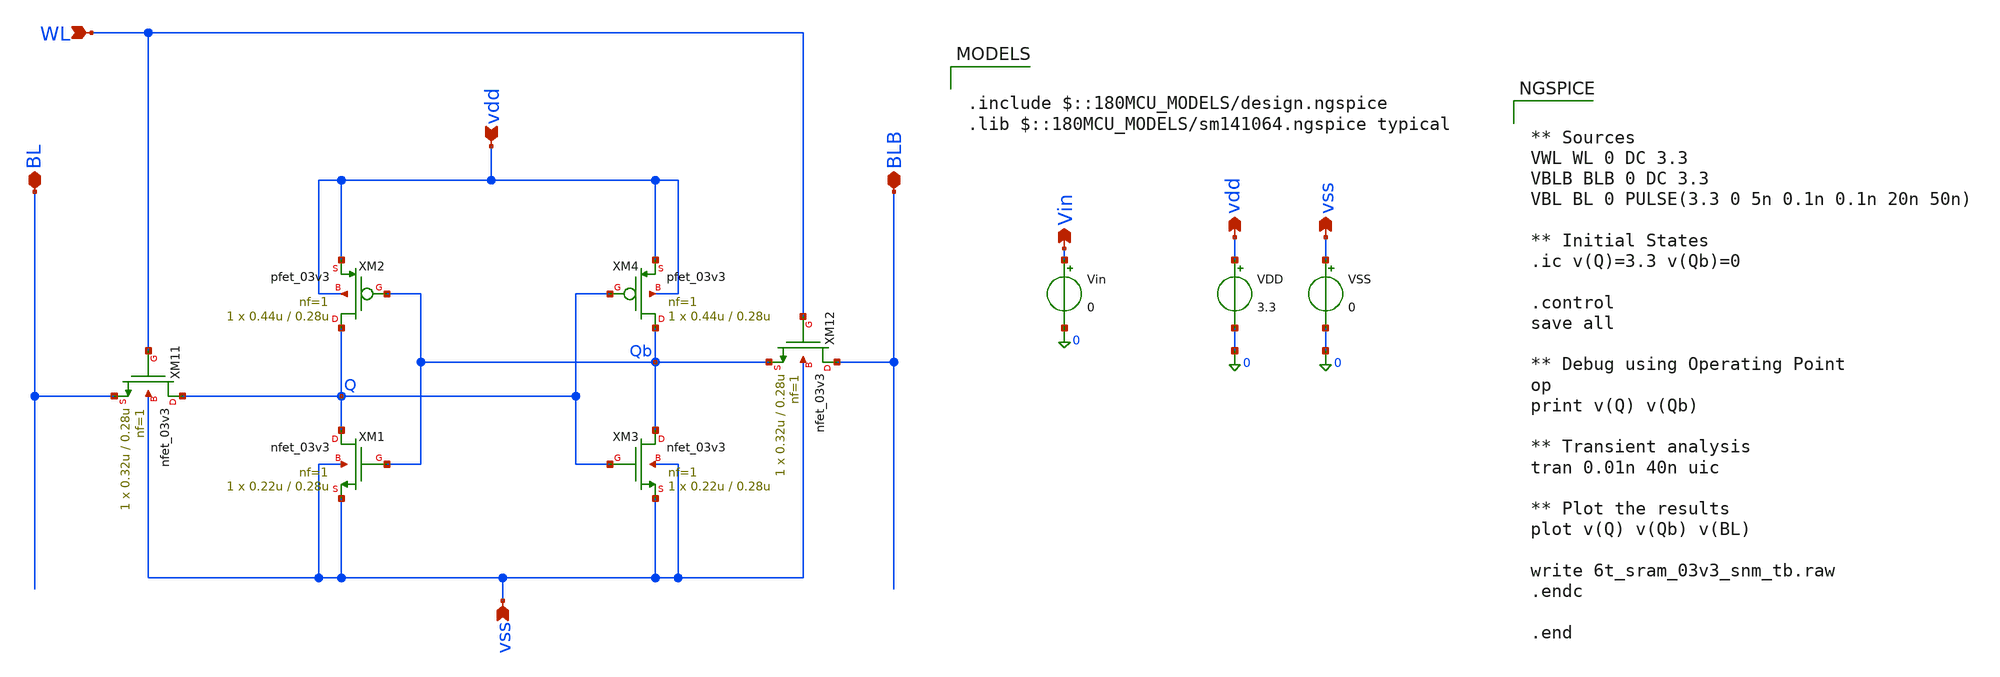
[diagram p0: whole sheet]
** sch_path: analog/tests/6t_sram_03v3_write_snm_tb.sch
**.subckt 6t_sram_03v3_write_snm_tb vdd vss vdd vss Vin BL WL BLB
*.ipin vdd
*.ipin vss
*.opin vdd
*.opin vss
*.opin Vin
*.iopin BL
*.ipin WL
*.iopin BLB
XM1 Q Qb vss vss nfet_03v3 L=0.28u W=0.22u nf=1 ad='int((nf+1)/2) * W/nf * 0.18u' as='int((nf+2)/2) * W/nf * 0.18u'
+ pd='2*int((nf+1)/2) * (W/nf + 0.18u)' ps='2*int((nf+2)/2) * (W/nf + 0.18u)' nrd='0.18u / W' nrs='0.18u / W'
+ sa=0 sb=0 sd=0 m=1
XM2 Q Qb vdd vdd pfet_03v3 L=0.28u W=0.44u nf=1 ad='int((nf+1)/2) * W/nf * 0.18u' as='int((nf+2)/2) * W/nf * 0.18u'
+ pd='2*int((nf+1)/2) * (W/nf + 0.18u)' ps='2*int((nf+2)/2) * (W/nf + 0.18u)' nrd='0.18u / W' nrs='0.18u / W'
+ sa=0 sb=0 sd=0 m=1
XM3 Qb Q vss vss nfet_03v3 L=0.28u W=0.22u nf=1 ad='int((nf+1)/2) * W/nf * 0.18u' as='int((nf+2)/2) * W/nf * 0.18u'
+ pd='2*int((nf+1)/2) * (W/nf + 0.18u)' ps='2*int((nf+2)/2) * (W/nf + 0.18u)' nrd='0.18u / W' nrs='0.18u / W'
+ sa=0 sb=0 sd=0 m=1
XM4 Qb Q vdd vdd pfet_03v3 L=0.28u W=0.44u nf=1 ad='int((nf+1)/2) * W/nf * 0.18u' as='int((nf+2)/2) * W/nf * 0.18u'
+ pd='2*int((nf+1)/2) * (W/nf + 0.18u)' ps='2*int((nf+2)/2) * (W/nf + 0.18u)' nrd='0.18u / W' nrs='0.18u / W'
+ sa=0 sb=0 sd=0 m=1
VDD vdd 0 3.3
VSS vss 0 0
Vin Vin 0 0
XM11 Q WL BL vss nfet_03v3 L=0.28u W=0.32u nf=1 ad='int((nf+1)/2) * W/nf * 0.18u' as='int((nf+2)/2) * W/nf * 0.18u'
+ pd='2*int((nf+1)/2) * (W/nf + 0.18u)' ps='2*int((nf+2)/2) * (W/nf + 0.18u)' nrd='0.18u / W' nrs='0.18u / W'
+ sa=0 sb=0 sd=0 m=1
XM12 BLB WL Qb vss nfet_03v3 L=0.28u W=0.32u nf=1 ad='int((nf+1)/2) * W/nf * 0.18u' as='int((nf+2)/2) * W/nf * 0.18u'
+ pd='2*int((nf+1)/2) * (W/nf + 0.18u)' ps='2*int((nf+2)/2) * (W/nf + 0.18u)' nrd='0.18u / W' nrs='0.18u / W'
+ sa=0 sb=0 sd=0 m=1
**** begin user architecture code

.include $::180MCU_MODELS/design.ngspice
.lib $::180MCU_MODELS/sm141064.ngspice typical



** Sources
VWL WL 0 DC 3.3
VBLB BLB 0 DC 3.3
VBL BL 0 PULSE(3.3 0 5n 0.1n 0.1n 20n 50n)

** Initial States
.ic v(Q)=3.3 v(Qb)=0

.control
save all

** Debug using Operating Point
op
print v(Q) v(Qb)

** Transient analysis
tran 0.01n 40n uic

** Plot the results
plot v(Q) v(Qb) v(BL)

write 6t_sram_03v3_snm_tb.raw
.endc

.end


**** end user architecture code
**.ends
.end
